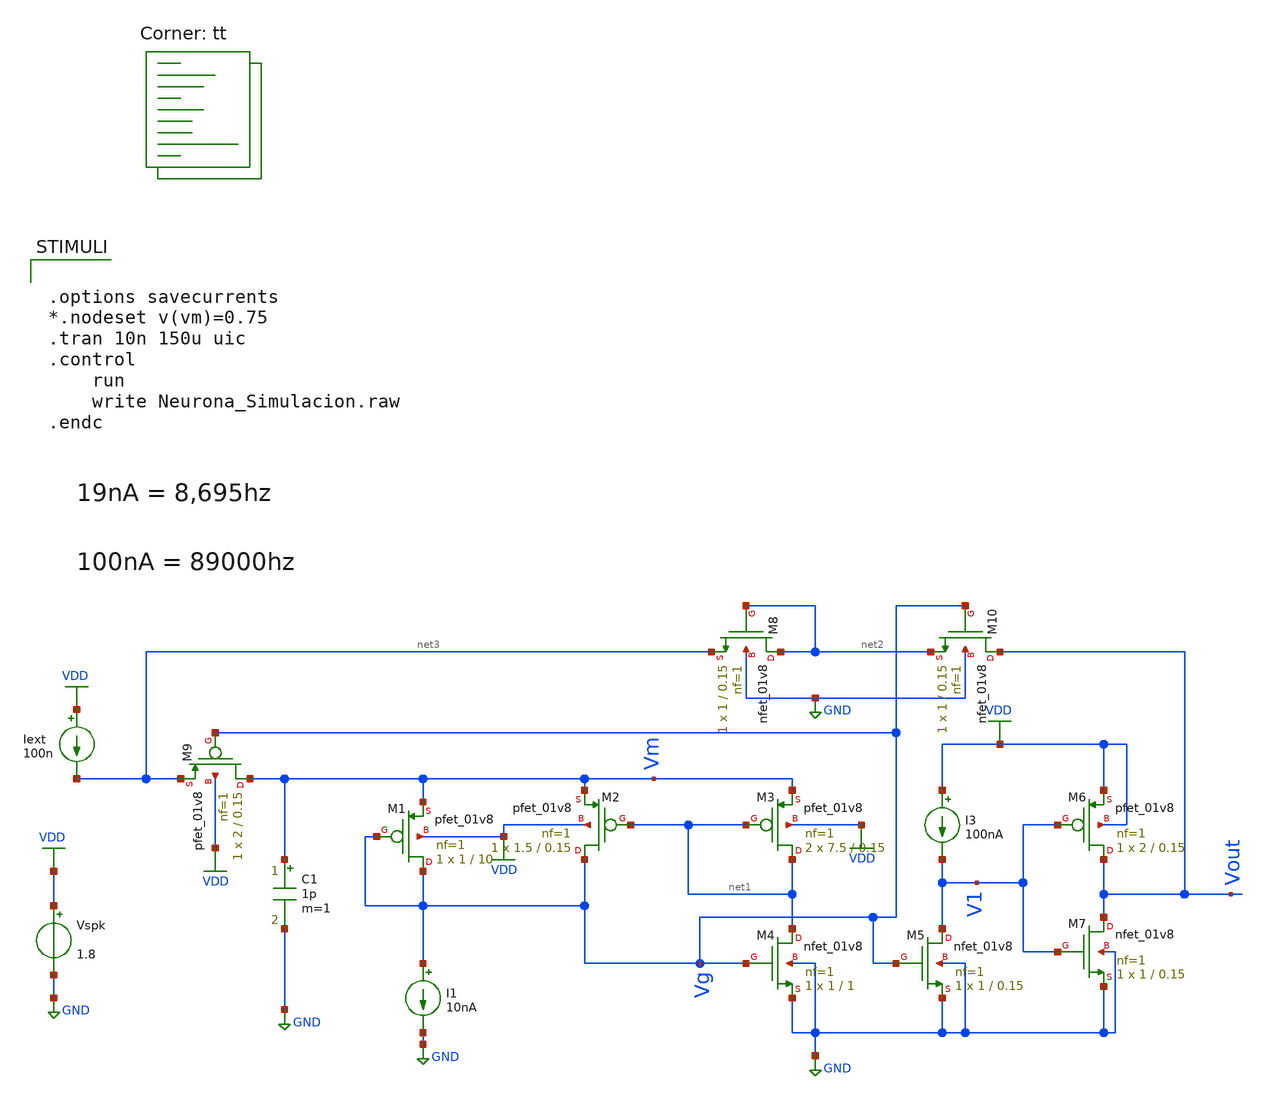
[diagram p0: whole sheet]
** sch_path: Neuron/ultralif/Neurona_Simulacion.sch
**.subckt Neurona_Simulacion
XM1 Vg Vg Vm VDD sky130_fd_pr__pfet_01v8 L=10 W=1 nf=1 ad='int((nf+1)/2) * W/nf * 0.29' as='int((nf+2)/2) * W/nf * 0.29'
+ pd='2*int((nf+1)/2) * (W/nf + 0.29)' ps='2*int((nf+2)/2) * (W/nf + 0.29)' nrd='0.29 / W' nrs='0.29 / W'
+ sa=0 sb=0 sd=0 mult=1 m=1
XM2 Vg net1 Vm VDD sky130_fd_pr__pfet_01v8 L=0.15 W=1.5 nf=1 ad='int((nf+1)/2) * W/nf * 0.29' as='int((nf+2)/2) * W/nf * 0.29'
+ pd='2*int((nf+1)/2) * (W/nf + 0.29)' ps='2*int((nf+2)/2) * (W/nf + 0.29)' nrd='0.29 / W' nrs='0.29 / W'
+ sa=0 sb=0 sd=0 mult=1 m=1
XM3 net1 net1 Vm VDD sky130_fd_pr__pfet_01v8 L=0.15 W=7.5 nf=1 ad='int((nf+1)/2) * W/nf * 0.29' as='int((nf+2)/2) * W/nf * 0.29'
+ pd='2*int((nf+1)/2) * (W/nf + 0.29)' ps='2*int((nf+2)/2) * (W/nf + 0.29)' nrd='0.29 / W' nrs='0.29 / W'
+ sa=0 sb=0 sd=0 mult=2 m=2
XM4 net1 Vg GND GND sky130_fd_pr__nfet_01v8 L=1 W=1 nf=1 ad='int((1 + 1)/2) * 1 / 1 * 0.29' as='int((1 + 2)/2) * 1 / 1 * 0.29'
+ pd='2*int((1 + 1)/2) * (1 / 1 + 0.29)' ps='2*int((1 + 2)/2) * (1 / 1 + 0.29)' nrd='0.29 / 1 ' nrs='0.29 / 1 '
+ sa=0 sb=0 sd=0 mult=1 m=1
XM5 V1 Vg GND GND sky130_fd_pr__nfet_01v8 L=0.15 W=1 nf=1 ad='int((1 + 1)/2) * 1 / 1 * 0.29' as='int((1 + 2)/2) * 1 / 1 * 0.29'
+ pd='2*int((1 + 1)/2) * (1 / 1 + 0.29)' ps='2*int((1 + 2)/2) * (1 / 1 + 0.29)' nrd='0.29 / 1 ' nrs='0.29 / 1 '
+ sa=0 sb=0 sd=0 mult=1 m=1
XM6 Vout V1 VDD VDD sky130_fd_pr__pfet_01v8 L=0.15 W=2 nf=1 ad='int((nf+1)/2) * W/nf * 0.29' as='int((nf+2)/2) * W/nf * 0.29'
+ pd='2*int((nf+1)/2) * (W/nf + 0.29)' ps='2*int((nf+2)/2) * (W/nf + 0.29)' nrd='0.29 / W' nrs='0.29 / W'
+ sa=0 sb=0 sd=0 mult=1 m=1
XM7 Vout V1 GND GND sky130_fd_pr__nfet_01v8 L=0.15 W=1 nf=1 ad='int((1 + 1)/2) * 1 / 1 * 0.29' as='int((1 + 2)/2) * 1 / 1 * 0.29'
+ pd='2*int((1 + 1)/2) * (1 / 1 + 0.29)' ps='2*int((1 + 2)/2) * (1 / 1 + 0.29)' nrd='0.29 / 1 ' nrs='0.29 / 1 '
+ sa=0 sb=0 sd=0 mult=1 m=1
I1 Vg GND 10nA
Vspk VDD GND 1.8
C1 Vm GND 1p m=1
Iext VDD net3 100n
I3 VDD V1 100nA
XM8 net2 net2 net3 GND sky130_fd_pr__nfet_01v8 L=0.15 W=1 nf=1 ad='int((1 + 1)/2) * 1 / 1 * 0.29' as='int((1 + 2)/2) * 1 / 1 * 0.29'
+ pd='2*int((1 + 1)/2) * (1 / 1 + 0.29)' ps='2*int((1 + 2)/2) * (1 / 1 + 0.29)' nrd='0.29 / 1 ' nrs='0.29 / 1 '
+ sa=0 sb=0 sd=0 mult=1 m=1
XM9 Vm Vg net3 VDD sky130_fd_pr__pfet_01v8 L=0.15 W=2 nf=1 ad='int((nf+1)/2) * W/nf * 0.29' as='int((nf+2)/2) * W/nf * 0.29'
+ pd='2*int((nf+1)/2) * (W/nf + 0.29)' ps='2*int((nf+2)/2) * (W/nf + 0.29)' nrd='0.29 / W' nrs='0.29 / W'
+ sa=0 sb=0 sd=0 mult=1 m=1
XM10 Vout Vg net2 GND sky130_fd_pr__nfet_01v8 L=0.15 W=1 nf=1 ad='int((1 + 1)/2) * 1 / 1 * 0.29' as='int((1 + 2)/2) * 1 / 1 * 0.29'
+ pd='2*int((1 + 1)/2) * (1 / 1 + 0.29)' ps='2*int((1 + 2)/2) * (1 / 1 + 0.29)' nrd='0.29 / 1 ' nrs='0.29 / 1 '
+ sa=0 sb=0 sd=0 mult=1 m=1
**** begin user architecture code
.lib $::SKYWATER_MODELS/sky130.lib.spice tt
**** end user architecture code
**.ends
.GLOBAL GND
.GLOBAL VDD
**** begin user architecture code


.options savecurrents
*.nodeset v(vm)=0.75
.tran 10n 150u uic
.control
	run
	write Neurona_Simulacion.raw
.endc


**** end user architecture code
.end
